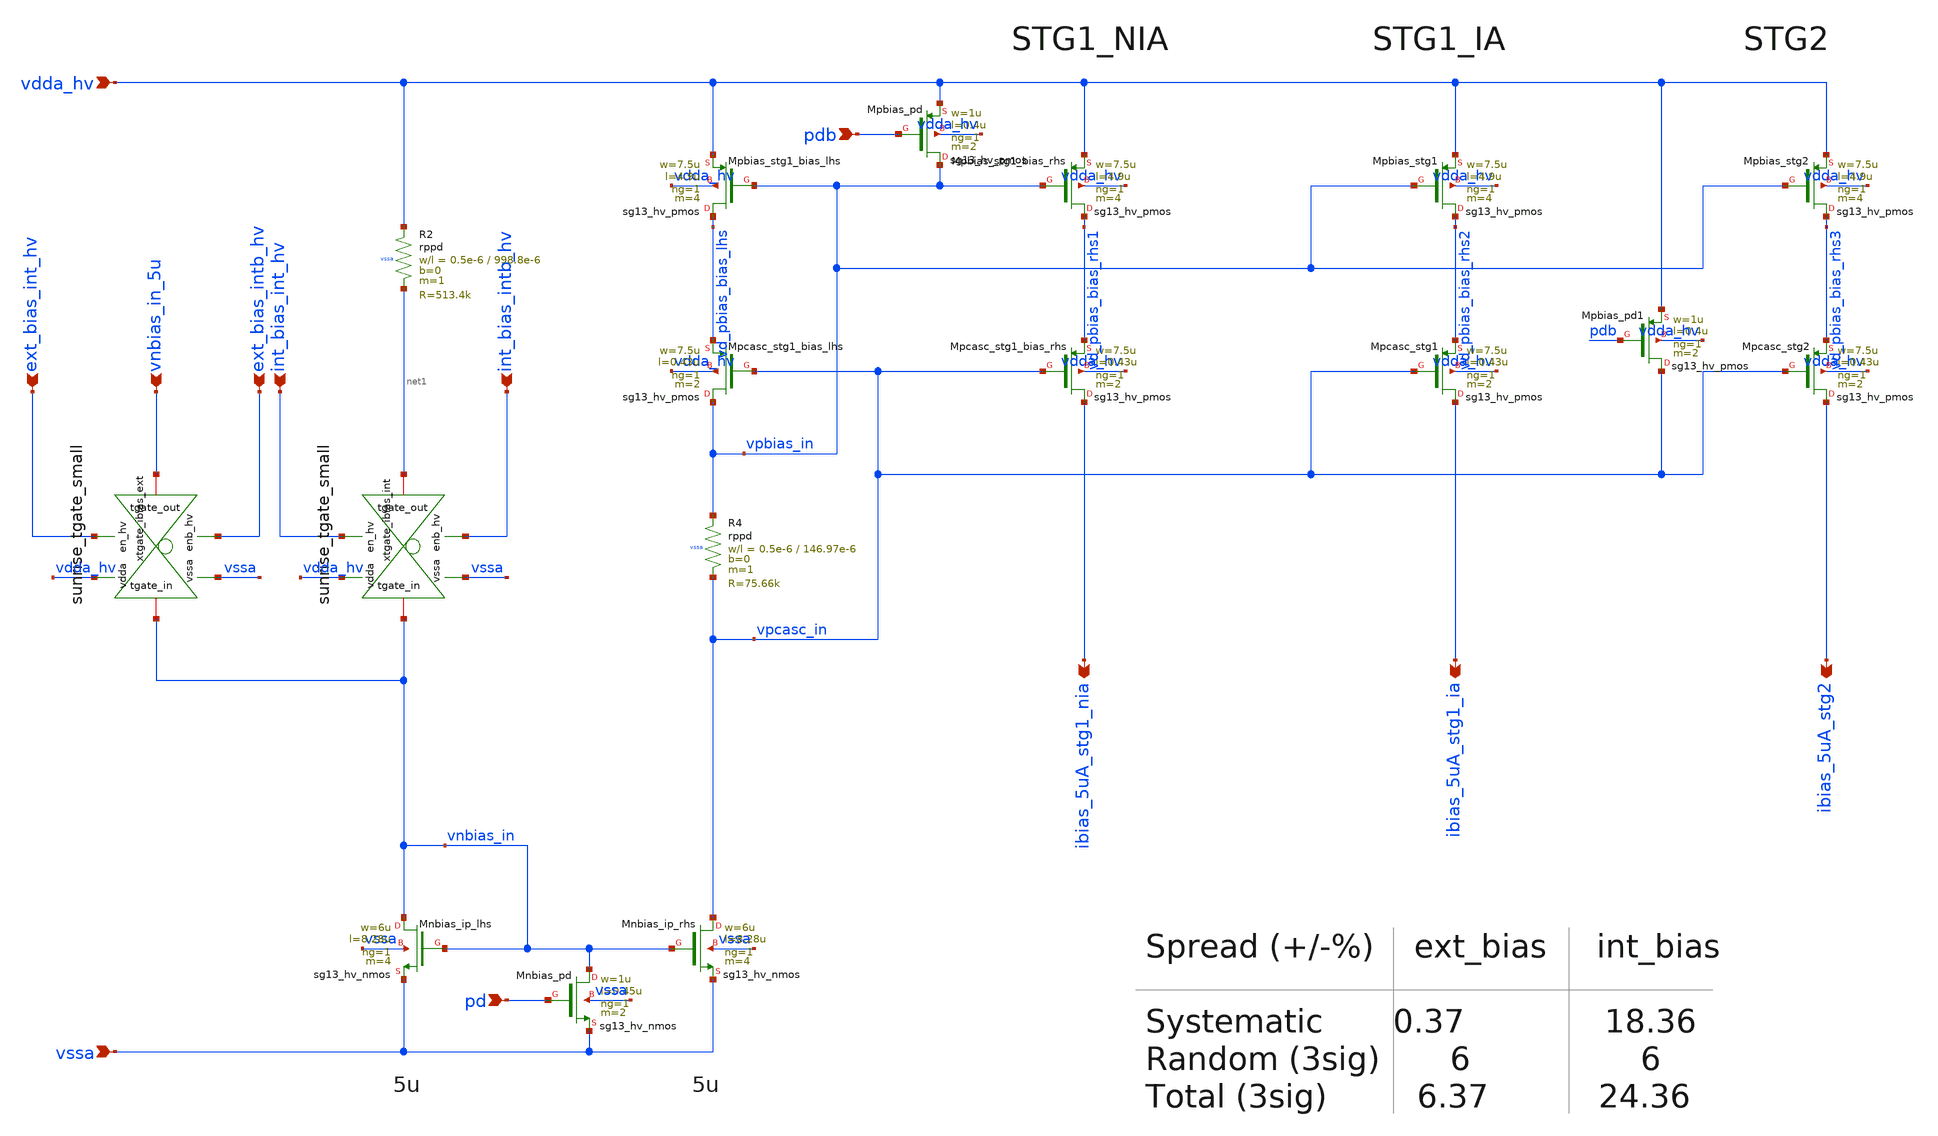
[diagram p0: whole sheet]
** sch_path: Schematics_Layout/sunrise_bias/sunrise_bias.sch
**.subckt sunrise_bias vssa vnbias_in_5u vdda_hv ibias_5uA_stg1_nia ibias_5uA_stg1_ia ibias_5uA_stg2
*+ ext_bias_intb_hv ext_bias_int_hv int_bias_intb_hv int_bias_int_hv pd pdb
*.ipin vssa
*.ipin vnbias_in_5u
*.ipin vdda_hv
*.opin ibias_5uA_stg1_nia
*.opin ibias_5uA_stg1_ia
*.opin ibias_5uA_stg2
*.ipin ext_bias_intb_hv
*.ipin ext_bias_int_hv
*.ipin int_bias_intb_hv
*.ipin int_bias_int_hv
*.ipin pd
*.ipin pdb
XMnbias_ip_lhs vnbias_in vnbias_in vssa vssa sg13_hv_nmos w=6u l=8.28u ng=1 m=4 mm_ok=1
XMnbias_ip_rhs vpcasc_in vnbias_in vssa vssa sg13_hv_nmos w=6u l=8.28u ng=1 m=4 mm_ok=1
XMpcasc_stg1_bias_lhs vpbias_in vpcasc_in vd_pbias_bias_lhs vdda_hv sg13_hv_pmos w=7.5u l=0.43u ng=1
+ m=2 mm_ok=1
XMpbias_stg1_bias_lhs vd_pbias_bias_lhs vpbias_in vdda_hv vdda_hv sg13_hv_pmos w=7.5u l=4.9u ng=1
+ m=4 mm_ok=1
XMpcasc_stg1_bias_rhs ibias_5uA_stg1_nia vpcasc_in vd_pbias_bias_rhs1 vdda_hv sg13_hv_pmos w=7.5u
+ l=0.43u ng=1 m=2 mm_ok=1
XMpbias_stg1_bias_rhs vd_pbias_bias_rhs1 vpbias_in vdda_hv vdda_hv sg13_hv_pmos w=7.5u l=4.9u ng=1
+ m=4 mm_ok=1
XR4 vpbias_in vpcasc_in vssa rppd w=0.5e-6 l=146.97e-6 m=1 b=0 mm_ok=1
XMpcasc_stg1 ibias_5uA_stg1_ia vpcasc_in vd_pbias_bias_rhs2 vdda_hv sg13_hv_pmos w=7.5u l=0.43u ng=1
+ m=2 mm_ok=1
XMpbias_stg1 vd_pbias_bias_rhs2 vpbias_in vdda_hv vdda_hv sg13_hv_pmos w=7.5u l=4.9u ng=1 m=4
+ mm_ok=1
XMpcasc_stg2 ibias_5uA_stg2 vpcasc_in vd_pbias_bias_rhs3 vdda_hv sg13_hv_pmos w=7.5u l=0.43u ng=1
+ m=2 mm_ok=1
XMpbias_stg2 vd_pbias_bias_rhs3 vpbias_in vdda_hv vdda_hv sg13_hv_pmos w=7.5u l=4.9u ng=1 m=4
+ mm_ok=1
xtgate_ibias_int vdda_hv vssa int_bias_int_hv vnbias_in net1 int_bias_intb_hv sunrise_tgate_small
XR2 vdda_hv net1 vssa rppd w=0.5e-6 l=998.8e-6 m=1 b=0 mm_ok=1
xtgate_ibias_ext vdda_hv vssa ext_bias_int_hv vnbias_in vnbias_in_5u ext_bias_intb_hv
+ sunrise_tgate_small
XMnbias_pd vnbias_in pd vssa vssa sg13_hv_nmos w=1u l=0.45u ng=1 m=2 mm_ok=1
XMpbias_pd vpbias_in pdb vdda_hv vdda_hv sg13_hv_pmos w=1u l=0.4u ng=1 m=2 mm_ok=1
XMpbias_pd1 vpcasc_in pdb vdda_hv vdda_hv sg13_hv_pmos w=1u l=0.4u ng=1 m=2 mm_ok=1
**.ends
.end
